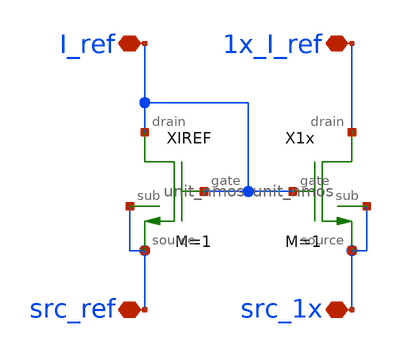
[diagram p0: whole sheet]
** sch_path: designs/libs/core_current_mirror/nmos_current_mirror_sources_io/nmos_current_mirror_sources_io.sch
**.subckt nmos_current_mirror_sources_io I_ref src_ref 1x_I_ref src_1x
*.iopin I_ref
*.iopin src_ref
*.iopin 1x_I_ref
*.iopin src_1x
XIREF I_ref src_ref I_ref src_ref unit_nmos M=1
X1x 1x_I_ref src_1x I_ref src_1x unit_nmos M=1
**.ends

* expanding   symbol:  libs/core_single_mos/unit_nmos/unit_nmos.sym # of pins=4
** sym_path: libs/core_single_mos/unit_nmos/unit_nmos.sym
** sch_path: libs/core_single_mos/unit_nmos/unit_nmos.sch
.subckt unit_nmos drain sub gate source
*.iopin drain
*.iopin source
*.iopin sub
*.iopin gate
XM1 drain gate source sub nfet_03v3 L=0.5u W=12u nf=2 ad='int((nf+1)/2) * W/nf * 0.18u' as='int((nf+2)/2) * W/nf * 0.18u'
+ pd='2*int((nf+1)/2) * (W/nf + 0.18u)' ps='2*int((nf+2)/2) * (W/nf + 0.18u)' nrd='0.18u / W' nrs='0.18u / W'
+ sa=0 sb=0 sd=0 m={M}
**** begin user architecture code

.param M=1

**** end user architecture code
.ends

.end
